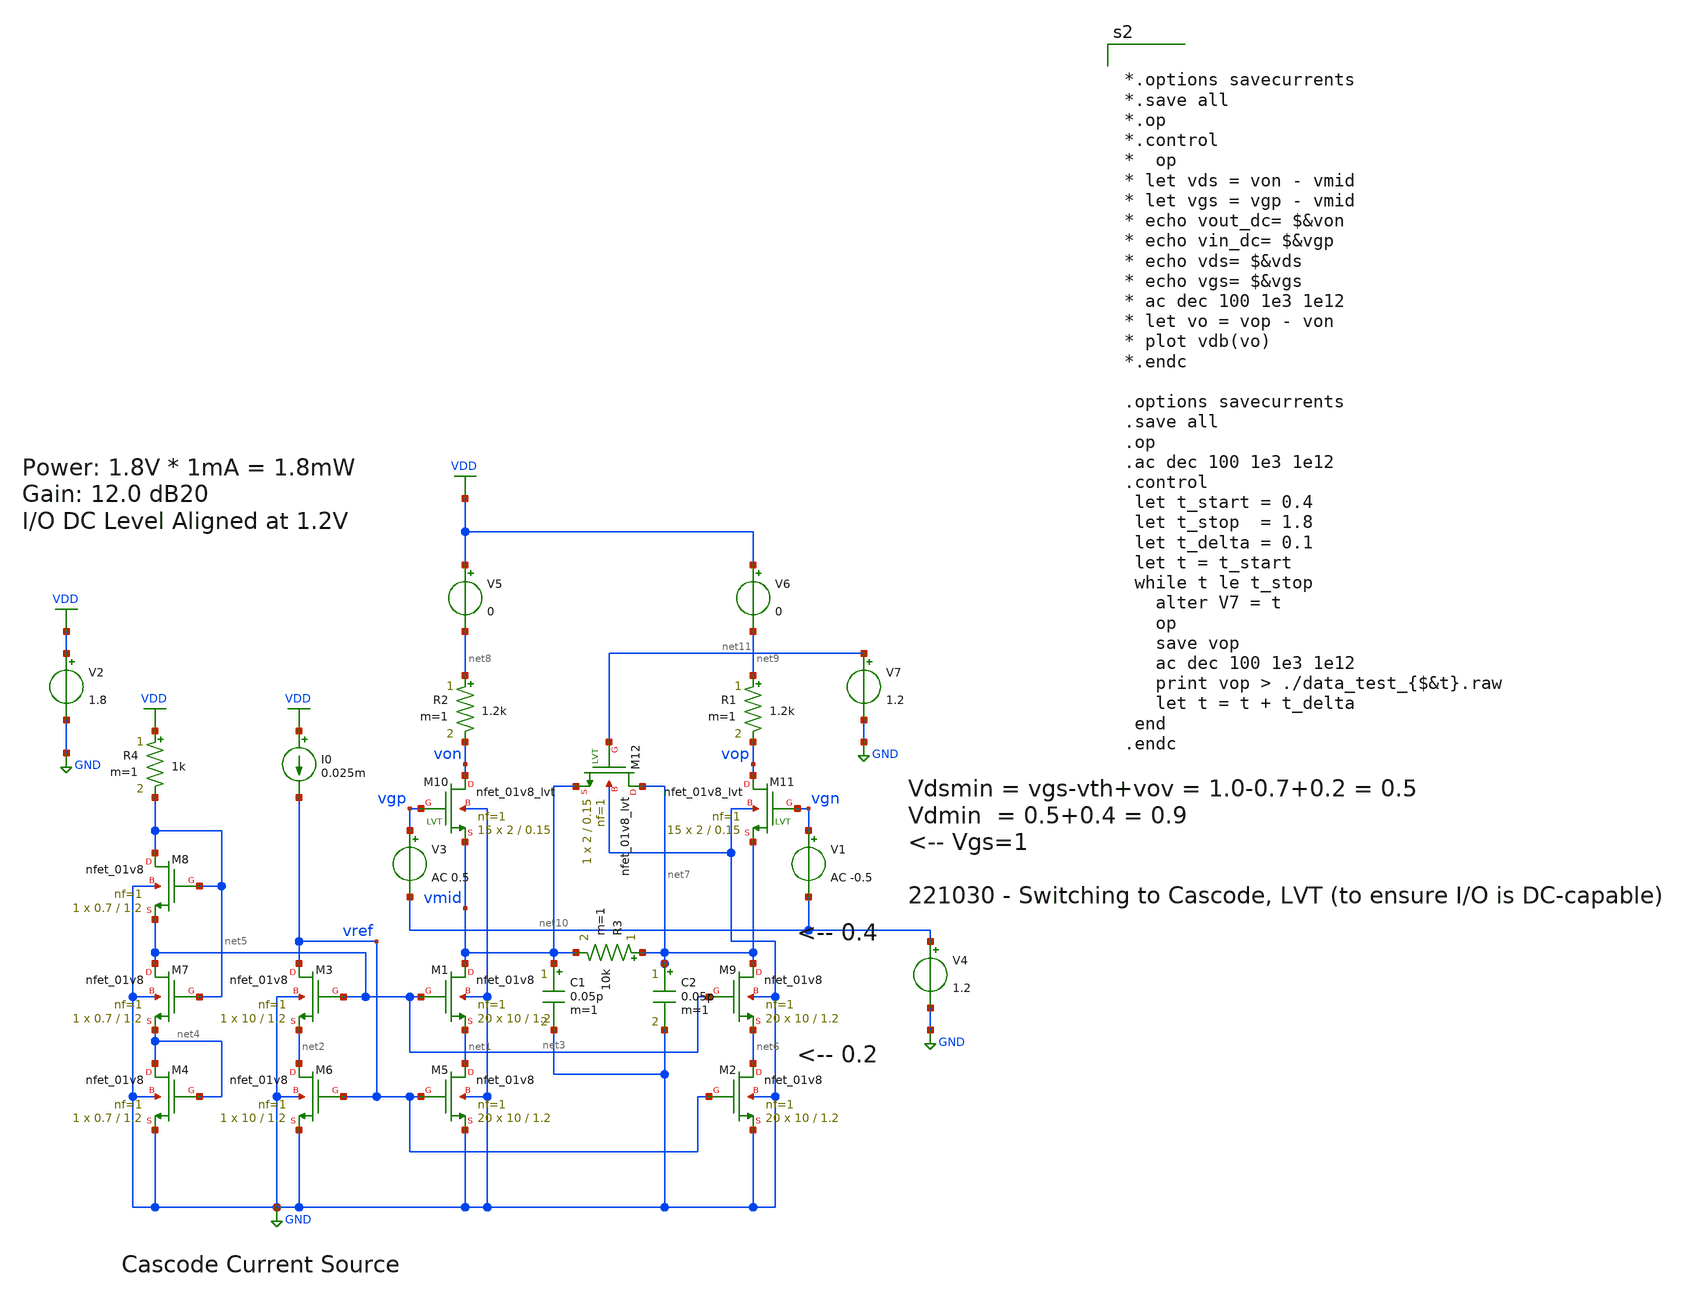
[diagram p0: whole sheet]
** sch_path: xschem/ctle_3.sch
**.subckt ctle_3
XM5 net1 vref GND GND sky130_fd_pr__nfet_01v8 L=1.2 W=10 nf=1 ad='int((nf+1)/2) * W/nf * 0.29' as='int((nf+2)/2) * W/nf * 0.29'
+ pd='2*int((nf+1)/2) * (W/nf + 0.29)' ps='2*int((nf+2)/2) * (W/nf + 0.29)' nrd='0.29 / W' nrs='0.29 / W'
+ sa=0 sb=0 sd=0 mult=20 m=20
XM6 net2 vref GND GND sky130_fd_pr__nfet_01v8 L=1.2 W=10 nf=1 ad='int((nf+1)/2) * W/nf * 0.29' as='int((nf+2)/2) * W/nf * 0.29'
+ pd='2*int((nf+1)/2) * (W/nf + 0.29)' ps='2*int((nf+2)/2) * (W/nf + 0.29)' nrd='0.29 / W' nrs='0.29 / W'
+ sa=0 sb=0 sd=0 mult=1 m=1
I0 VDD vref 0.025m
XM1 vmid net3 net1 GND sky130_fd_pr__nfet_01v8 L=1.2 W=10 nf=1 ad='int((nf+1)/2) * W/nf * 0.29' as='int((nf+2)/2) * W/nf * 0.29'
+ pd='2*int((nf+1)/2) * (W/nf + 0.29)' ps='2*int((nf+2)/2) * (W/nf + 0.29)' nrd='0.29 / W' nrs='0.29 / W'
+ sa=0 sb=0 sd=0 mult=20 m=20
XM3 vref net3 net2 GND sky130_fd_pr__nfet_01v8 L=1.2 W=10 nf=1 ad='int((nf+1)/2) * W/nf * 0.29' as='int((nf+2)/2) * W/nf * 0.29'
+ pd='2*int((nf+1)/2) * (W/nf + 0.29)' ps='2*int((nf+2)/2) * (W/nf + 0.29)' nrd='0.29 / W' nrs='0.29 / W'
+ sa=0 sb=0 sd=0 mult=1 m=1
XM4 net4 net4 GND GND sky130_fd_pr__nfet_01v8 L=1.2 W=0.7 nf=1 ad='int((nf+1)/2) * W/nf * 0.29' as='int((nf+2)/2) * W/nf * 0.29'
+ pd='2*int((nf+1)/2) * (W/nf + 0.29)' ps='2*int((nf+2)/2) * (W/nf + 0.29)' nrd='0.29 / W' nrs='0.29 / W'
+ sa=0 sb=0 sd=0 mult=1 m=1
XM7 net3 net5 net4 GND sky130_fd_pr__nfet_01v8 L=1.2 W=0.7 nf=1 ad='int((nf+1)/2) * W/nf * 0.29' as='int((nf+2)/2) * W/nf * 0.29'
+ pd='2*int((nf+1)/2) * (W/nf + 0.29)' ps='2*int((nf+2)/2) * (W/nf + 0.29)' nrd='0.29 / W' nrs='0.29 / W'
+ sa=0 sb=0 sd=0 mult=1 m=1
XM8 net5 net5 net3 GND sky130_fd_pr__nfet_01v8 L=1.2 W=0.7 nf=1 ad='int((nf+1)/2) * W/nf * 0.29' as='int((nf+2)/2) * W/nf * 0.29'
+ pd='2*int((nf+1)/2) * (W/nf + 0.29)' ps='2*int((nf+2)/2) * (W/nf + 0.29)' nrd='0.29 / W' nrs='0.29 / W'
+ sa=0 sb=0 sd=0 mult=1 m=1
XM2 net6 vref GND GND sky130_fd_pr__nfet_01v8 L=1.2 W=10 nf=1 ad='int((nf+1)/2) * W/nf * 0.29' as='int((nf+2)/2) * W/nf * 0.29'
+ pd='2*int((nf+1)/2) * (W/nf + 0.29)' ps='2*int((nf+2)/2) * (W/nf + 0.29)' nrd='0.29 / W' nrs='0.29 / W'
+ sa=0 sb=0 sd=0 mult=20 m=20
XM9 net7 net3 net6 GND sky130_fd_pr__nfet_01v8 L=1.2 W=10 nf=1 ad='int((nf+1)/2) * W/nf * 0.29' as='int((nf+2)/2) * W/nf * 0.29'
+ pd='2*int((nf+1)/2) * (W/nf + 0.29)' ps='2*int((nf+2)/2) * (W/nf + 0.29)' nrd='0.29 / W' nrs='0.29 / W'
+ sa=0 sb=0 sd=0 mult=20 m=20
V2 VDD GND 1.8
XM10 von vgp vmid GND sky130_fd_pr__nfet_01v8_lvt L=0.15 W=2 nf=1 ad='int((nf+1)/2) * W/nf * 0.29' as='int((nf+2)/2) * W/nf * 0.29'
+ pd='2*int((nf+1)/2) * (W/nf + 0.29)' ps='2*int((nf+2)/2) * (W/nf + 0.29)' nrd='0.29 / W' nrs='0.29 / W'
+ sa=0 sb=0 sd=0 mult=15 m=15
XM11 vop vgn net7 GND sky130_fd_pr__nfet_01v8_lvt L=0.15 W=2 nf=1 ad='int((nf+1)/2) * W/nf * 0.29' as='int((nf+2)/2) * W/nf * 0.29'
+ pd='2*int((nf+1)/2) * (W/nf + 0.29)' ps='2*int((nf+2)/2) * (W/nf + 0.29)' nrd='0.29 / W' nrs='0.29 / W'
+ sa=0 sb=0 sd=0 mult=15 m=15
V3 vgp net10 AC 0.5
V4 net10 GND 1.2
V1 vgn net10 AC -0.5
R1 net9 vop 1.2k m=1
R2 net8 von 1.2k m=1
C1 vmid GND 0.05p m=1
C2 net7 GND 0.05p m=1
V5 VDD net8 0
V6 VDD net9 0
R3 net7 vmid 10k m=1
R4 VDD net5 1k m=1
XM12 net7 net11 vmid GND sky130_fd_pr__nfet_01v8_lvt L=0.15 W=2 nf=1 ad='int((nf+1)/2) * W/nf * 0.29'
+ as='int((nf+2)/2) * W/nf * 0.29' pd='2*int((nf+1)/2) * (W/nf + 0.29)' ps='2*int((nf+2)/2) * (W/nf + 0.29)'
+ nrd='0.29 / W' nrs='0.29 / W' sa=0 sb=0 sd=0 mult=1 m=1
V7 net11 GND 1.2
**** begin user architecture code
.lib $::SKYWATER_MODELS/sky130.lib.spice tt
* .include $::PDKPATH/libs.ref/sky130_fd_sc_hvl/spice/sky130_fd_sc_hvl.spice



*.options savecurrents
*.save all
*.op
*.control
*  op
* let vds = von - vmid
* let vgs = vgp - vmid
* echo vout_dc= $&von
* echo vin_dc= $&vgp
* echo vds= $&vds
* echo vgs= $&vgs
* ac dec 100 1e3 1e12
* let vo = vop - von
* plot vdb(vo)
*.endc

.options savecurrents
.save all
.op
.ac dec 100 1e3 1e12
.control
 let t_start = 0.4
 let t_stop  = 1.8
 let t_delta = 0.1
 let t = t_start
 while t le t_stop
   alter V7 = t
   op
   save vop
   ac dec 100 1e3 1e12
   print vop > ./data_test_{$&t}.raw
   let t = t + t_delta
 end
.endc



**** end user architecture code
**.ends
.GLOBAL GND
.GLOBAL VDD
.end
